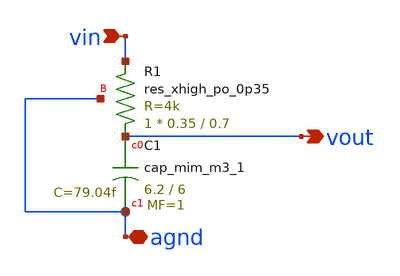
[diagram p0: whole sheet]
** sch_path: AMP/LPF.sch
**.subckt LPF vin vout agnd
*.ipin vin
*.opin vout
*.iopin agnd
XC1 vout agnd sky130_fd_pr__cap_mim_m3_1 W=6.2 L=6 MF=1 m=1
XR1 vout vin agnd sky130_fd_pr__res_xhigh_po_0p35 L=0.7 mult=1 m=1
**.ends
.end
